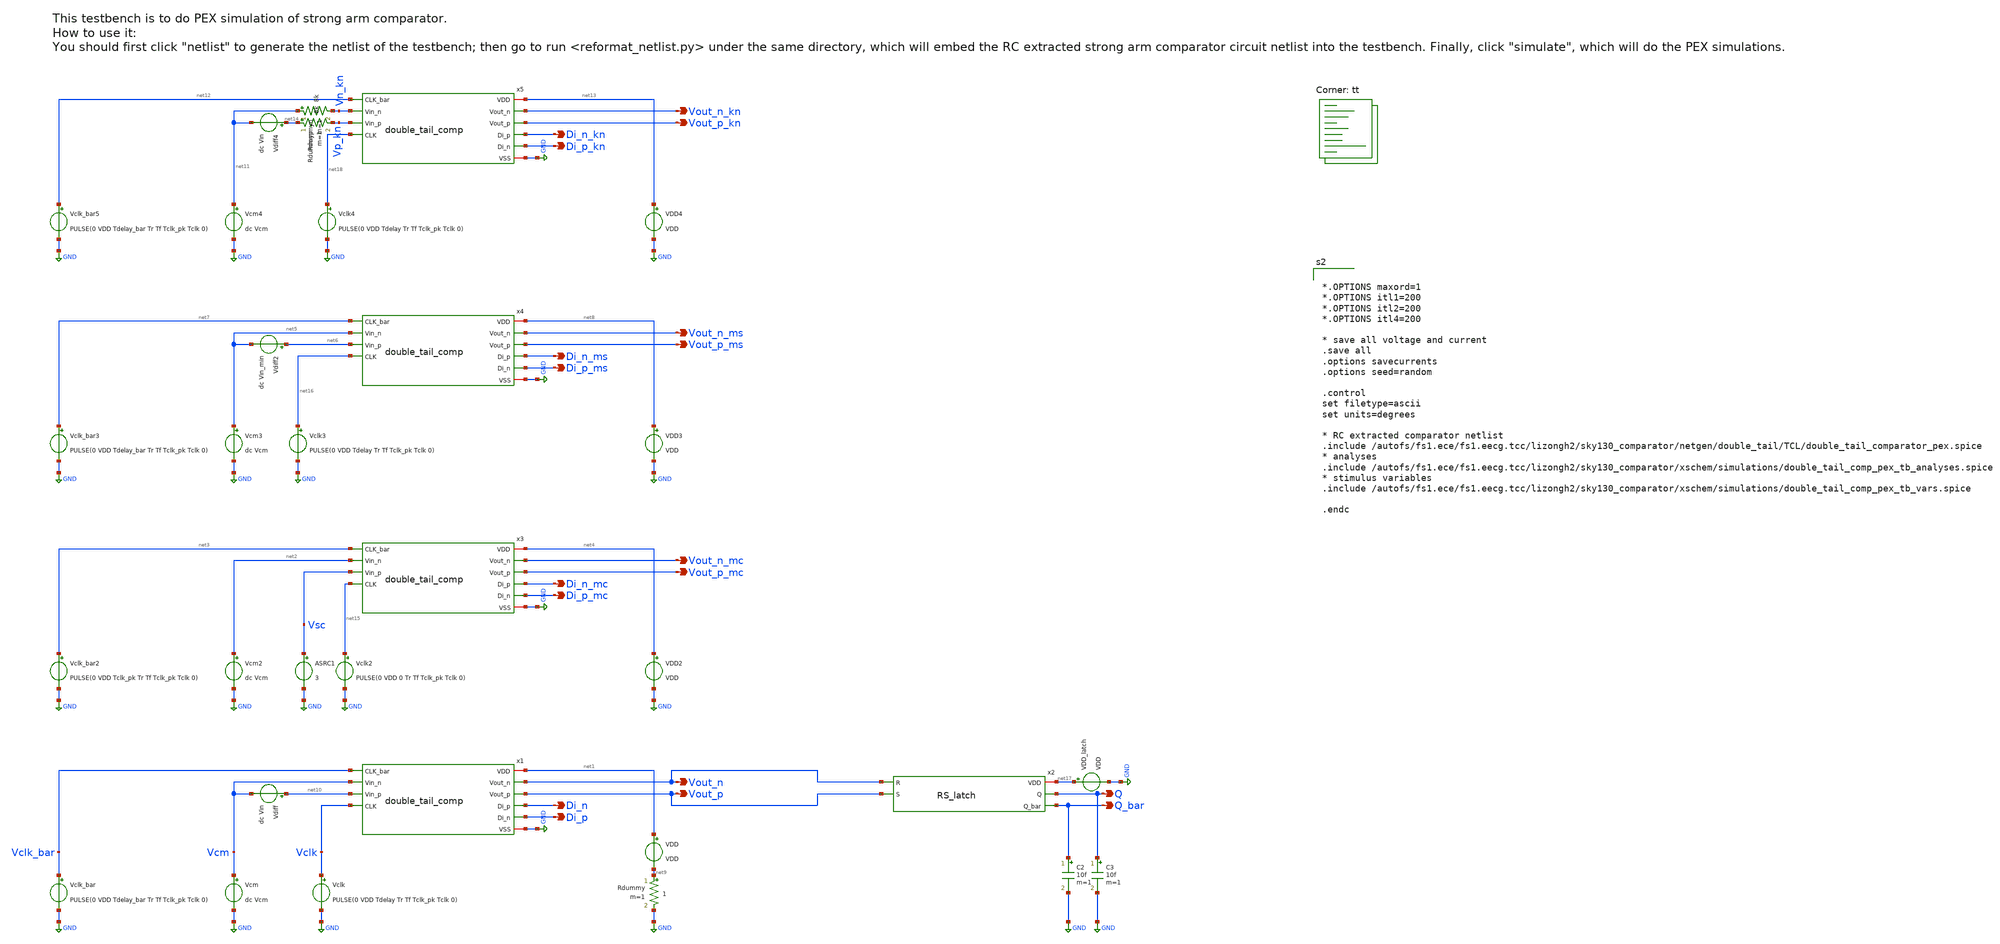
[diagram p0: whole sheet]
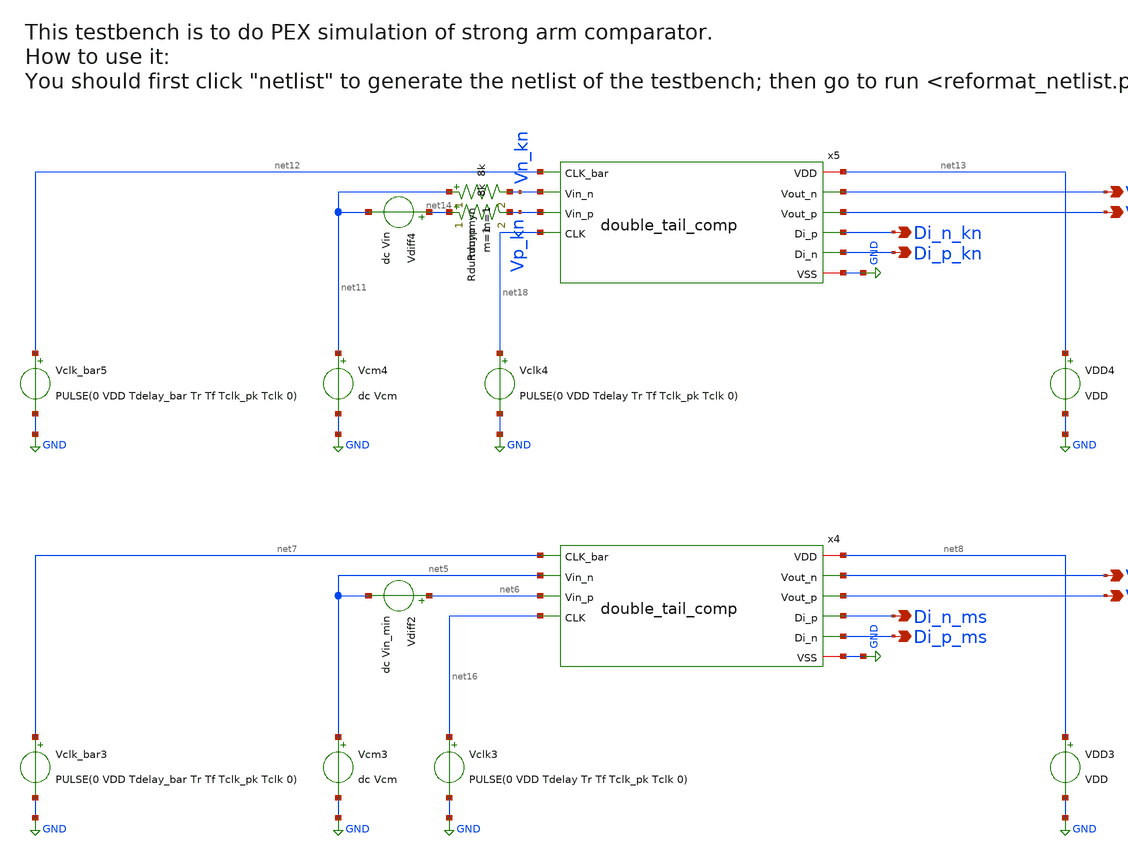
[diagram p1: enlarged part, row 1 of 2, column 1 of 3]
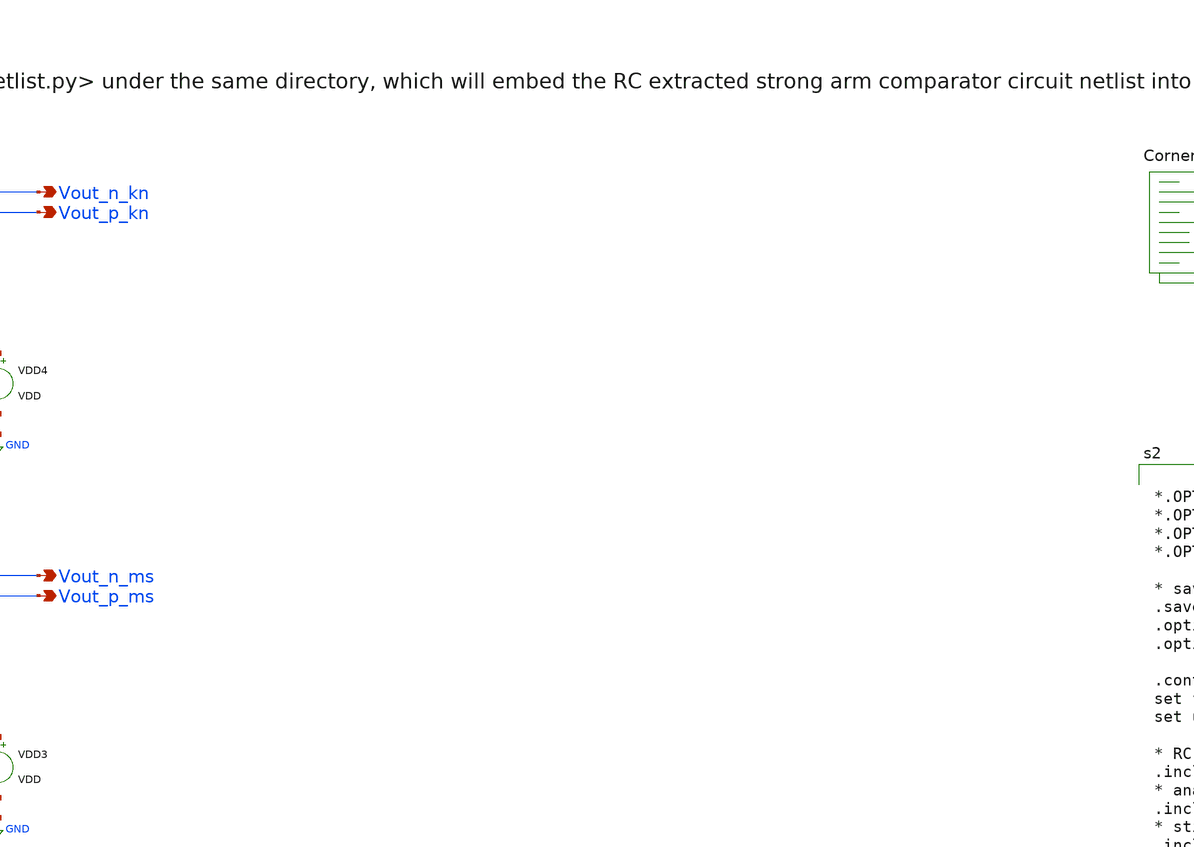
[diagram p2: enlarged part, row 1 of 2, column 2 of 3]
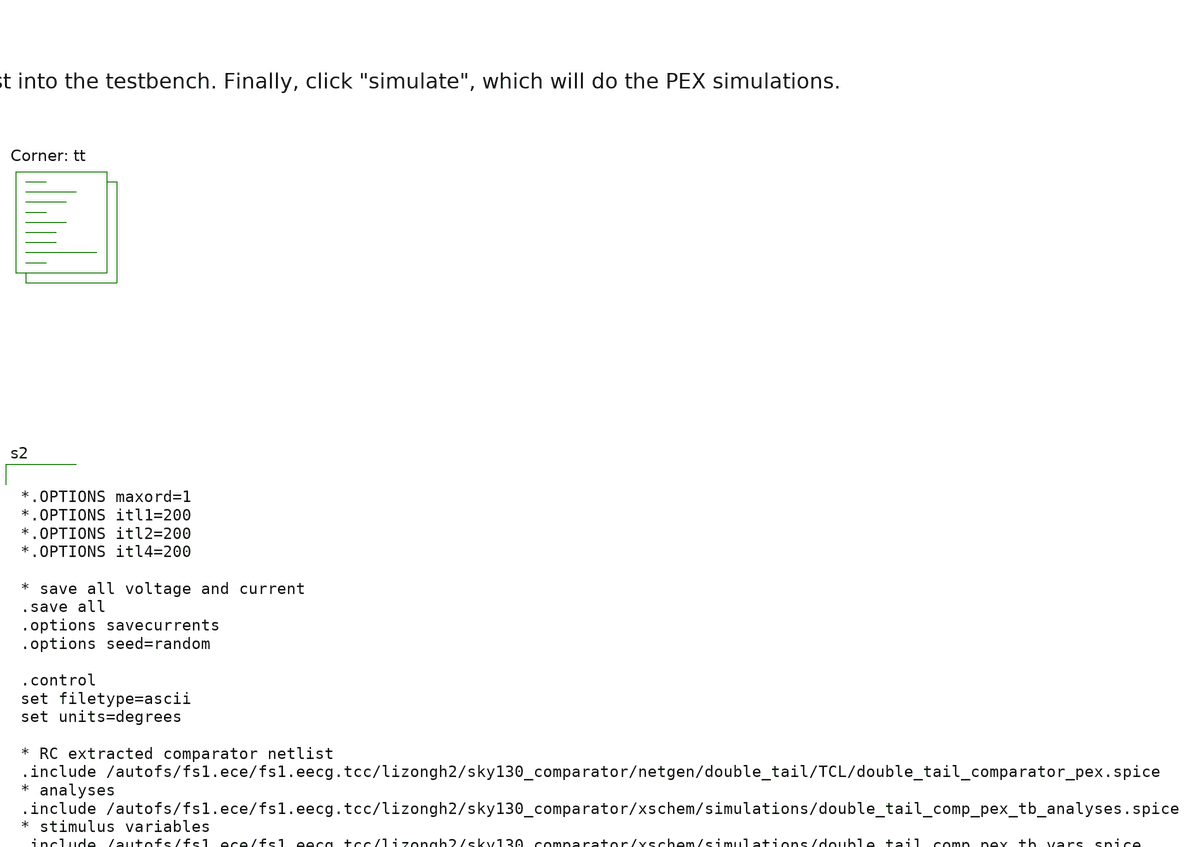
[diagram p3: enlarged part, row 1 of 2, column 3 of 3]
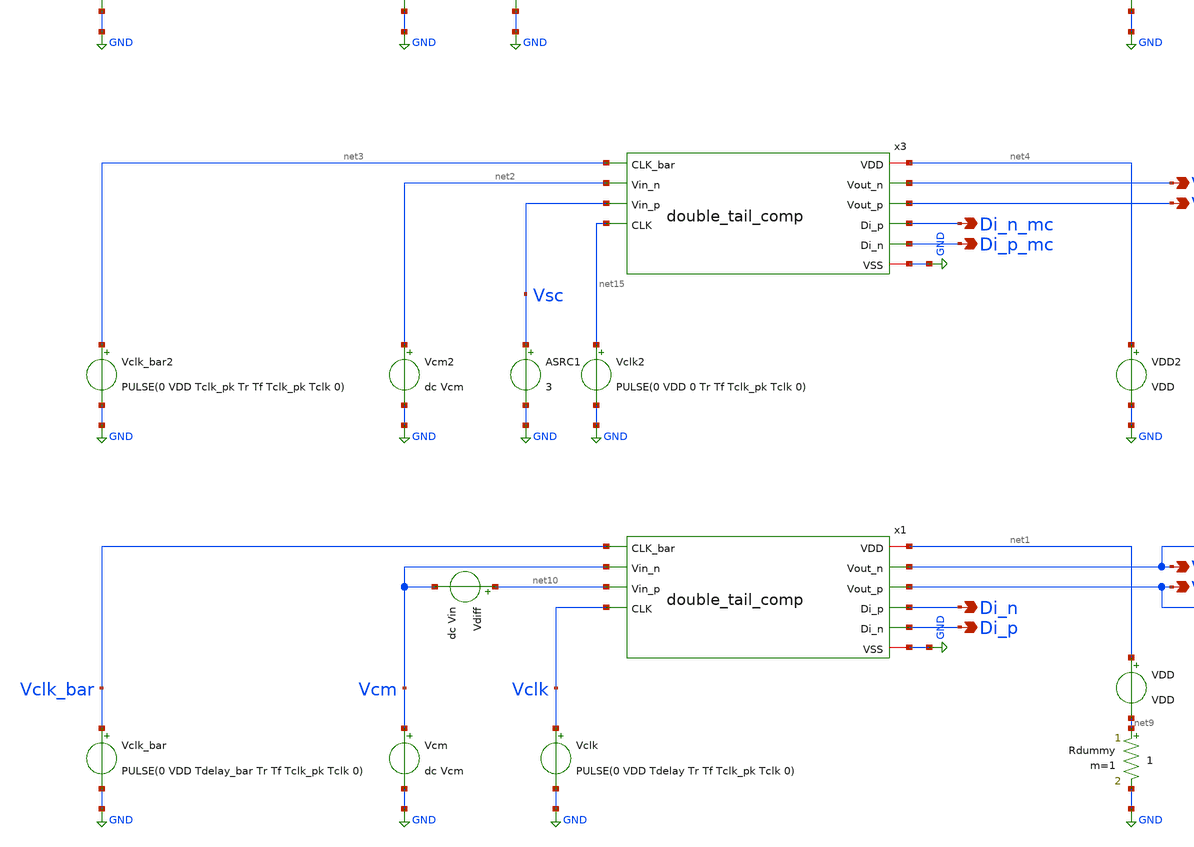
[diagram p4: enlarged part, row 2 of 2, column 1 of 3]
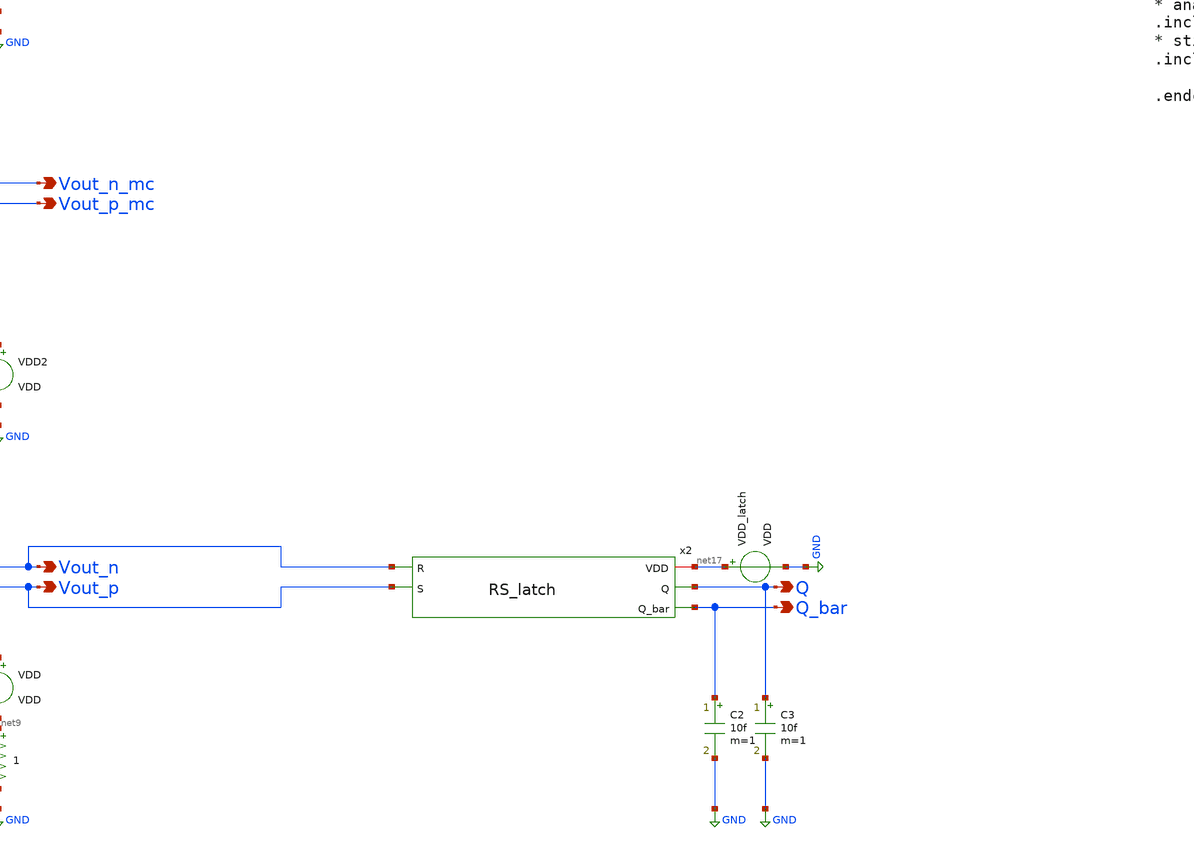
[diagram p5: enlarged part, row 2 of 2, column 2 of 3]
** sch_path: xschem/double_tail_comp_pex_tb.sch
**.subckt double_tail_comp_pex_tb Di_n Di_p Vout_n Vout_p Q Q_bar Di_n_mc Di_p_mc Vout_n_mc
*+ Vout_p_mc Di_n_ms Di_p_ms Vout_n_ms Vout_p_ms Di_n_kn Di_p_kn Vout_n_kn Vout_p_kn
*.opin Di_n
*.opin Di_p
*.opin Vout_n
*.opin Vout_p
*.opin Q
*.opin Q_bar
*.opin Di_n_mc
*.opin Di_p_mc
*.opin Vout_n_mc
*.opin Vout_p_mc
*.opin Di_n_ms
*.opin Di_p_ms
*.opin Vout_n_ms
*.opin Vout_p_ms
*.opin Di_n_kn
*.opin Di_p_kn
*.opin Vout_n_kn
*.opin Vout_p_kn
x1 net1 Vclk_bar Vout_n Vout_p Di_n Di_p Vcm net10 Vclk GND double_tail_comp
VDD net1 net9 VDD
Vclk Vclk GND PULSE(0 VDD Tdelay Tr Tf Tclk_pk Tclk 0)
Vclk_bar Vclk_bar GND PULSE(0 VDD Tdelay_bar Tr Tf Tclk_pk Tclk 0)
Vcm Vcm GND dc Vcm
Vdiff net10 Vcm dc Vin
C2 Q_bar GND 10f m=1
C3 Q GND 10f m=1
x2 net17 Vout_n Q Vout_p Q_bar RS_latch
x3 net4 net3 Vout_n_mc Vout_p_mc Di_n_mc Di_p_mc net2 Vsc net15 GND double_tail_comp
VDD2 net4 GND VDD
Vclk2 net15 GND PULSE(0 VDD 0 Tr Tf Tclk_pk Tclk 0)
Vclk_bar2 net3 GND PULSE(0 VDD Tclk_pk Tr Tf Tclk_pk Tclk 0)
Vcm2 net2 GND dc Vcm
ASRC1 %v([ Vsc ]) filesrc
x4 net8 net7 Vout_n_ms Vout_p_ms Di_n_ms Di_p_ms net5 net6 net16 GND double_tail_comp
VDD3 net8 GND VDD
Vclk3 net16 GND PULSE(0 VDD Tdelay Tr Tf Tclk_pk Tclk 0)
Vclk_bar3 net7 GND PULSE(0 VDD Tdelay_bar Tr Tf Tclk_pk Tclk 0)
Vcm3 net5 GND dc Vcm
Vdiff2 net6 net5 dc Vin_min
VDD_latch net17 GND VDD
Rdummy net9 GND 1 m=1
x5 net13 net12 Vout_n_kn Vout_p_kn Di_n_kn Di_p_kn Vn_kn Vp_kn net18 GND double_tail_comp
VDD4 net13 GND VDD
Vclk4 net18 GND PULSE(0 VDD Tdelay Tr Tf Tclk_pk Tclk 0)
Vclk_bar5 net12 GND PULSE(0 VDD Tdelay_bar Tr Tf Tclk_pk Tclk 0)
Vcm4 net11 GND dc Vcm
Vdiff4 net14 net11 dc Vin
Rdummyn net11 Vn_kn 8k m=1
Rdummyp net14 Vp_kn 8k m=1
**** begin user architecture code
.lib $::SKYWATER_MODELS/sky130.lib.spice tt


*.OPTIONS maxord=1
*.OPTIONS itl1=200
*.OPTIONS itl2=200
*.OPTIONS itl4=200

* save all voltage and current
.save all
.options savecurrents
.options seed=random

.control
set filetype=ascii
set units=degrees

* RC extracted comparator netlist
.include /autofs/fs1.ece/fs1.eecg.tcc/lizongh2/sky130_comparator/netgen/double_tail/TCL/double_tail_comparator_pex.spice
* analyses
.include /autofs/fs1.ece/fs1.eecg.tcc/lizongh2/sky130_comparator/xschem/simulations/double_tail_comp_pex_tb_analyses.spice
* stimulus variables
.include /autofs/fs1.ece/fs1.eecg.tcc/lizongh2/sky130_comparator/xschem/simulations/double_tail_comp_pex_tb_vars.spice

.endc


**** end user architecture code
**.ends

* expanding   symbol:  double_tail_comp.sym # of pins=10
** sym_path: xschem/double_tail_comp.sym
** sch_path: xschem/double_tail_comp.sch
.subckt double_tail_comp VDD CLK_bar Vout_n Vout_p Di_p Di_n Vin_n Vin_p CLK VSS
*.ipin CLK
*.ipin Vin_p
*.ipin Vin_n
*.opin Di_n
*.opin Di_p
*.opin Vout_n
*.opin Vout_p
*.ipin CLK_bar
*.iopin VDD
*.iopin VSS
XM1 Di_n Vin_p net1 VSS sky130_fd_pr__nfet_01v8 L=0.15 W=W_M1 nf=10 ad='int((nf+1)/2) * W/nf * 0.29'
+ as='int((nf+2)/2) * W/nf * 0.29' pd='2*int((nf+1)/2) * (W/nf + 0.29)' ps='2*int((nf+2)/2) * (W/nf + 0.29)'
+ nrd='0.29 / W' nrs='0.29 / W' sa=0 sb=0 sd=0 mult=1 m=1
XM2 Di_p Vin_n net1 VSS sky130_fd_pr__nfet_01v8 L=0.15 W=W_M2 nf=10 ad='int((nf+1)/2) * W/nf * 0.29'
+ as='int((nf+2)/2) * W/nf * 0.29' pd='2*int((nf+1)/2) * (W/nf + 0.29)' ps='2*int((nf+2)/2) * (W/nf + 0.29)'
+ nrd='0.29 / W' nrs='0.29 / W' sa=0 sb=0 sd=0 mult=1 m=1
XM3 Di_n CLK VDD VDD sky130_fd_pr__pfet_01v8 L=0.15 W=W_M3 nf=2 ad='int((nf+1)/2) * W/nf * 0.29' as='int((nf+2)/2) * W/nf * 0.29'
+ pd='2*int((nf+1)/2) * (W/nf + 0.29)' ps='2*int((nf+2)/2) * (W/nf + 0.29)' nrd='0.29 / W' nrs='0.29 / W'
+ sa=0 sb=0 sd=0 mult=1 m=1
XM4 Di_p CLK VDD VDD sky130_fd_pr__pfet_01v8 L=0.15 W=W_M4 nf=2 ad='int((nf+1)/2) * W/nf * 0.29' as='int((nf+2)/2) * W/nf * 0.29'
+ pd='2*int((nf+1)/2) * (W/nf + 0.29)' ps='2*int((nf+2)/2) * (W/nf + 0.29)' nrd='0.29 / W' nrs='0.29 / W'
+ sa=0 sb=0 sd=0 mult=1 m=1
XM5 net1 CLK VSS VSS sky130_fd_pr__nfet_01v8 L=0.15 W=W_M5 nf=12 ad='int((nf+1)/2) * W/nf * 0.29' as='int((nf+2)/2) * W/nf * 0.29'
+ pd='2*int((nf+1)/2) * (W/nf + 0.29)' ps='2*int((nf+2)/2) * (W/nf + 0.29)' nrd='0.29 / W' nrs='0.29 / W'
+ sa=0 sb=0 sd=0 mult=1 m=1
XM6 Vout_p Di_n VSS VSS sky130_fd_pr__nfet_01v8 L=0.15 W=W_M6 nf=4 ad='int((nf+1)/2) * W/nf * 0.29' as='int((nf+2)/2) * W/nf * 0.29'
+ pd='2*int((nf+1)/2) * (W/nf + 0.29)' ps='2*int((nf+2)/2) * (W/nf + 0.29)' nrd='0.29 / W' nrs='0.29 / W'
+ sa=0 sb=0 sd=0 mult=1 m=1
XM7 Vout_p Vout_n VSS VSS sky130_fd_pr__nfet_01v8 L=0.15 W=W_M7 nf=2 ad='int((nf+1)/2) * W/nf * 0.29'
+ as='int((nf+2)/2) * W/nf * 0.29' pd='2*int((nf+1)/2) * (W/nf + 0.29)' ps='2*int((nf+2)/2) * (W/nf + 0.29)'
+ nrd='0.29 / W' nrs='0.29 / W' sa=0 sb=0 sd=0 mult=1 m=1
XM8 Vout_n Vout_p VSS VSS sky130_fd_pr__nfet_01v8 L=0.15 W=W_M8 nf=2 ad='int((nf+1)/2) * W/nf * 0.29'
+ as='int((nf+2)/2) * W/nf * 0.29' pd='2*int((nf+1)/2) * (W/nf + 0.29)' ps='2*int((nf+2)/2) * (W/nf + 0.29)'
+ nrd='0.29 / W' nrs='0.29 / W' sa=0 sb=0 sd=0 mult=1 m=1
XM9 Vout_n Di_p VSS VSS sky130_fd_pr__nfet_01v8 L=0.15 W=W_M9 nf=4 ad='int((nf+1)/2) * W/nf * 0.29' as='int((nf+2)/2) * W/nf * 0.29'
+ pd='2*int((nf+1)/2) * (W/nf + 0.29)' ps='2*int((nf+2)/2) * (W/nf + 0.29)' nrd='0.29 / W' nrs='0.29 / W'
+ sa=0 sb=0 sd=0 mult=1 m=1
XM10 Vout_p Vout_n net2 VDD sky130_fd_pr__pfet_01v8 L=0.15 W=W_M10 nf=2 ad='int((nf+1)/2) * W/nf * 0.29'
+ as='int((nf+2)/2) * W/nf * 0.29' pd='2*int((nf+1)/2) * (W/nf + 0.29)' ps='2*int((nf+2)/2) * (W/nf + 0.29)'
+ nrd='0.29 / W' nrs='0.29 / W' sa=0 sb=0 sd=0 mult=1 m=1
XM11 Vout_n Vout_p net2 VDD sky130_fd_pr__pfet_01v8 L=0.15 W=W_M11 nf=2 ad='int((nf+1)/2) * W/nf * 0.29'
+ as='int((nf+2)/2) * W/nf * 0.29' pd='2*int((nf+1)/2) * (W/nf + 0.29)' ps='2*int((nf+2)/2) * (W/nf + 0.29)'
+ nrd='0.29 / W' nrs='0.29 / W' sa=0 sb=0 sd=0 mult=1 m=1
XM12 net2 CLK_bar VDD VDD sky130_fd_pr__pfet_01v8 L=0.15 W=W_M12 nf=12 ad='int((nf+1)/2) * W/nf * 0.29'
+ as='int((nf+2)/2) * W/nf * 0.29' pd='2*int((nf+1)/2) * (W/nf + 0.29)' ps='2*int((nf+2)/2) * (W/nf + 0.29)'
+ nrd='0.29 / W' nrs='0.29 / W' sa=0 sb=0 sd=0 mult=1 m=1
.ends


* expanding   symbol:  RS_latch.sym # of pins=5
** sym_path: xschem/RS_latch.sym
** sch_path: xschem/RS_latch.sch
.subckt RS_latch VDD R Q S Q_bar
*.iopin VDD
*.opin Q
*.opin Q_bar
*.ipin R
*.ipin S
x1 VDD R Q_bar Q nor
x2 VDD Q S Q_bar nor
.ends


* expanding   symbol:  nor.sym # of pins=4
** sym_path: xschem/nor.sym
** sch_path: xschem/nor.sch
.subckt nor VDD A B out
*.iopin VDD
*.ipin A
*.ipin B
*.opin out
XM1 out B GND GND sky130_fd_pr__nfet_01v8 L=0.15 W=0.42 nf=1 ad='int((nf+1)/2) * W/nf * 0.29' as='int((nf+2)/2) * W/nf * 0.29'
+ pd='2*int((nf+1)/2) * (W/nf + 0.29)' ps='2*int((nf+2)/2) * (W/nf + 0.29)' nrd='0.29 / W' nrs='0.29 / W'
+ sa=0 sb=0 sd=0 mult=1 m=1
XM2 out A GND GND sky130_fd_pr__nfet_01v8 L=0.15 W=0.42 nf=1 ad='int((nf+1)/2) * W/nf * 0.29' as='int((nf+2)/2) * W/nf * 0.29'
+ pd='2*int((nf+1)/2) * (W/nf + 0.29)' ps='2*int((nf+2)/2) * (W/nf + 0.29)' nrd='0.29 / W' nrs='0.29 / W'
+ sa=0 sb=0 sd=0 mult=1 m=1
XM3 out B net1 VDD sky130_fd_pr__pfet_01v8 L=0.15 W=0.84 nf=1 ad='int((nf+1)/2) * W/nf * 0.29' as='int((nf+2)/2) * W/nf * 0.29'
+ pd='2*int((nf+1)/2) * (W/nf + 0.29)' ps='2*int((nf+2)/2) * (W/nf + 0.29)' nrd='0.29 / W' nrs='0.29 / W'
+ sa=0 sb=0 sd=0 mult=1 m=1
XM4 net1 A VDD VDD sky130_fd_pr__pfet_01v8 L=0.15 W=0.84 nf=1 ad='int((nf+1)/2) * W/nf * 0.29' as='int((nf+2)/2) * W/nf * 0.29'
+ pd='2*int((nf+1)/2) * (W/nf + 0.29)' ps='2*int((nf+2)/2) * (W/nf + 0.29)' nrd='0.29 / W' nrs='0.29 / W'
+ sa=0 sb=0 sd=0 mult=1 m=1
.ends

.GLOBAL GND
**** begin user architecture code

.model filesrc filesource (file="staircase_voltage.txt" amploffset=[Vcm] amplscale=[1] timeoffset=0
+ timescale=1 timerelative=false amplstep=false)

**** end user architecture code
.end
